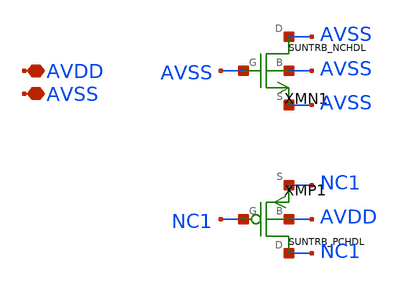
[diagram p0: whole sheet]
** sch_path: ip/sun_trb_sky130nm/design/SUN_TRB_SKY130NM/SUNTRB_TAPCELLBAVSS_CV.sch
**.subckt SUNTRB_TAPCELLBAVSS_CV AVDD AVSS
*.iopin AVDD
*.iopin AVSS
XMN1 AVSS AVSS AVSS AVSS SUNTRB_NCHDL xoffset=0 yoffset=0 angle=0
XMP1 NC1 NC1 NC1 AVDD SUNTRB_PCHDL xoffset=0 yoffset=0 angle=0
**.ends
.end
